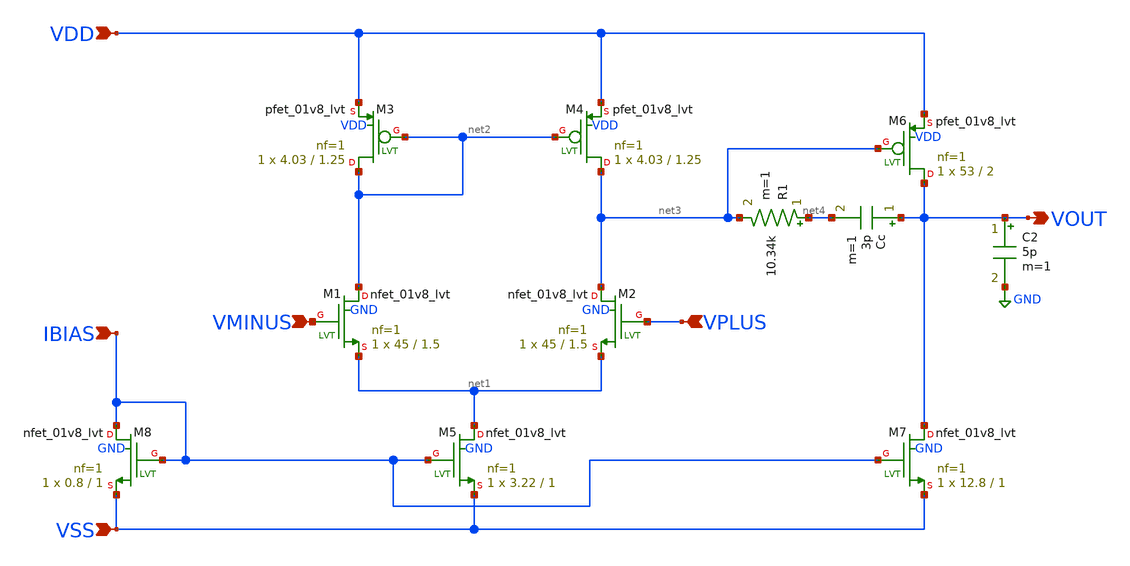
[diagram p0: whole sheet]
** sch_path: final.sch
**.subckt final VDD VMINUS VPLUS IBIAS VOUT VSS
*.ipin VDD
*.ipin VMINUS
*.ipin VPLUS
*.ipin IBIAS
*.opin VOUT
*.ipin VSS
Cc VOUT net4 3p m=1
XM5 net1 IBIAS VSS GND sky130_fd_pr__nfet_01v8_lvt L=1 W=3.22 nf=1 ad='int((1 + 1)/2) * 3.22 / 1 * 0.29'
+ as='int((1 + 2)/2) * 3.22 / 1 * 0.29' pd='2*int((1 + 1)/2) * (3.22 / 1 + 0.29)' ps='2*int((1 + 2)/2) * (3.22 / 1 + 0.29)'
+ nrd='0.29 / 3.22 ' nrs='0.29 / 3.22 ' sa=0 sb=0 sd=0 mult=1 m=1
XM8 IBIAS IBIAS VSS GND sky130_fd_pr__nfet_01v8_lvt L=1 W=0.8 nf=1 ad='int((1 + 1)/2) * 0.8 / 1 * 0.29'
+ as='int((1 + 2)/2) * 0.8 / 1 * 0.29' pd='2*int((1 + 1)/2) * (0.8 / 1 + 0.29)' ps='2*int((1 + 2)/2) * (0.8 / 1 + 0.29)'
+ nrd='0.29 / 0.8 ' nrs='0.29 / 0.8 ' sa=0 sb=0 sd=0 mult=1 m=1
XM1 net2 VMINUS net1 GND sky130_fd_pr__nfet_01v8_lvt L=1.5 W=45 nf=1 ad='int((1 + 1)/2) * 45 / 1 * 0.29'
+ as='int((1 + 2)/2) * 45 / 1 * 0.29' pd='2*int((1 + 1)/2) * (45 / 1 + 0.29)' ps='2*int((1 + 2)/2) * (45 / 1 + 0.29)'
+ nrd='0.29 / 45 ' nrs='0.29 / 45 ' sa=0 sb=0 sd=0 mult=1 m=1
XM2 net3 VPLUS net1 GND sky130_fd_pr__nfet_01v8_lvt L=1.5 W=45 nf=1 ad='int((1 + 1)/2) * 45 / 1 * 0.29'
+ as='int((1 + 2)/2) * 45 / 1 * 0.29' pd='2*int((1 + 1)/2) * (45 / 1 + 0.29)' ps='2*int((1 + 2)/2) * (45 / 1 + 0.29)'
+ nrd='0.29 / 45 ' nrs='0.29 / 45 ' sa=0 sb=0 sd=0 mult=1 m=1
XM4 net3 net2 VDD VDD sky130_fd_pr__pfet_01v8_lvt L=1.25 W=4.03 nf=1 ad='int((1 + 1)/2) * 4.03 / 1 * 0.29'
+ as='int((1 + 2)/2) * 4.03 / 1 * 0.29' pd='2*int((1 + 1)/2) * (4.03 / 1 + 0.29)' ps='2*int((1 + 2)/2) * (4.03 / 1 + 0.29)'
+ nrd='0.29 / 4.03 ' nrs='0.29 / 4.03 ' sa=0 sb=0 sd=0 mult=1 m=1
XM3 net2 net2 VDD VDD sky130_fd_pr__pfet_01v8_lvt L=1.25 W=4.03 nf=1 ad='int((1 + 1)/2) * 4.03 / 1 * 0.29'
+ as='int((1 + 2)/2) * 4.03 / 1 * 0.29' pd='2*int((1 + 1)/2) * (4.03 / 1 + 0.29)' ps='2*int((1 + 2)/2) * (4.03 / 1 + 0.29)'
+ nrd='0.29 / 4.03 ' nrs='0.29 / 4.03 ' sa=0 sb=0 sd=0 mult=1 m=1
XM7 VOUT IBIAS VSS GND sky130_fd_pr__nfet_01v8_lvt L=1 W=12.8 nf=1 ad='int((1 + 1)/2) * 12.8 / 1 * 0.29'
+ as='int((1 + 2)/2) * 12.8 / 1 * 0.29' pd='2*int((1 + 1)/2) * (12.8 / 1 + 0.29)' ps='2*int((1 + 2)/2) * (12.8 / 1 + 0.29)'
+ nrd='0.29 / 12.8 ' nrs='0.29 / 12.8 ' sa=0 sb=0 sd=0 mult=1 m=1
XM6 VOUT net3 VDD VDD sky130_fd_pr__pfet_01v8_lvt L=2 W=53 nf=1 ad='int((1 + 1)/2) * 53 / 1 * 0.29' as='int((1 + 2)/2) * 53 / 1 * 0.29'
+ pd='2*int((1 + 1)/2) * (53 / 1 + 0.29)' ps='2*int((1 + 2)/2) * (53 / 1 + 0.29)' nrd='0.29 / 53 ' nrs='0.29 / 53 '
+ sa=0 sb=0 sd=0 mult=1 m=1
C2 VOUT GND 5p m=1
R1 net4 net3 10.34k m=1
**.ends
.GLOBAL GND
.end
